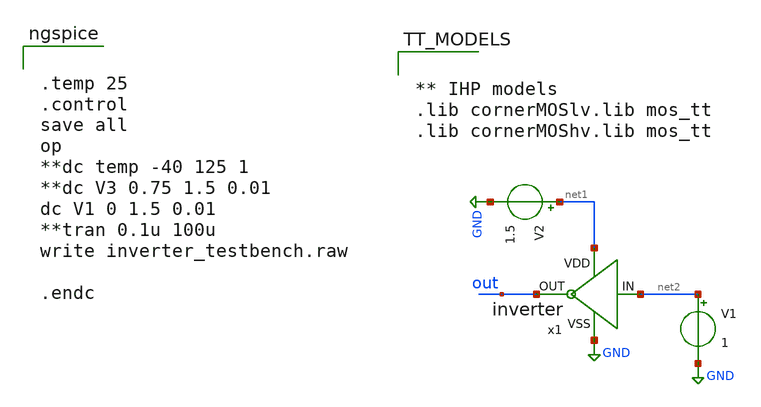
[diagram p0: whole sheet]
** sch_path: 10_xschem/inverter_testbench.sch
**.subckt inverter_testbench
x1 net1 net2 out GND inverter
V2 net1 GND 1.5
V1 net2 GND 1
**** begin user architecture code


.temp 25
.control
save all
op
**dc temp -40 125 1
**dc V3 0.75 1.5 0.01
dc V1 0 1.5 0.01
**tran 0.1u 100u
write inverter_testbench.raw

.endc




** IHP models
.lib cornerMOSlv.lib mos_tt
.lib cornerMOShv.lib mos_tt


**** end user architecture code
**.ends
.GLOBAL GND
.end
